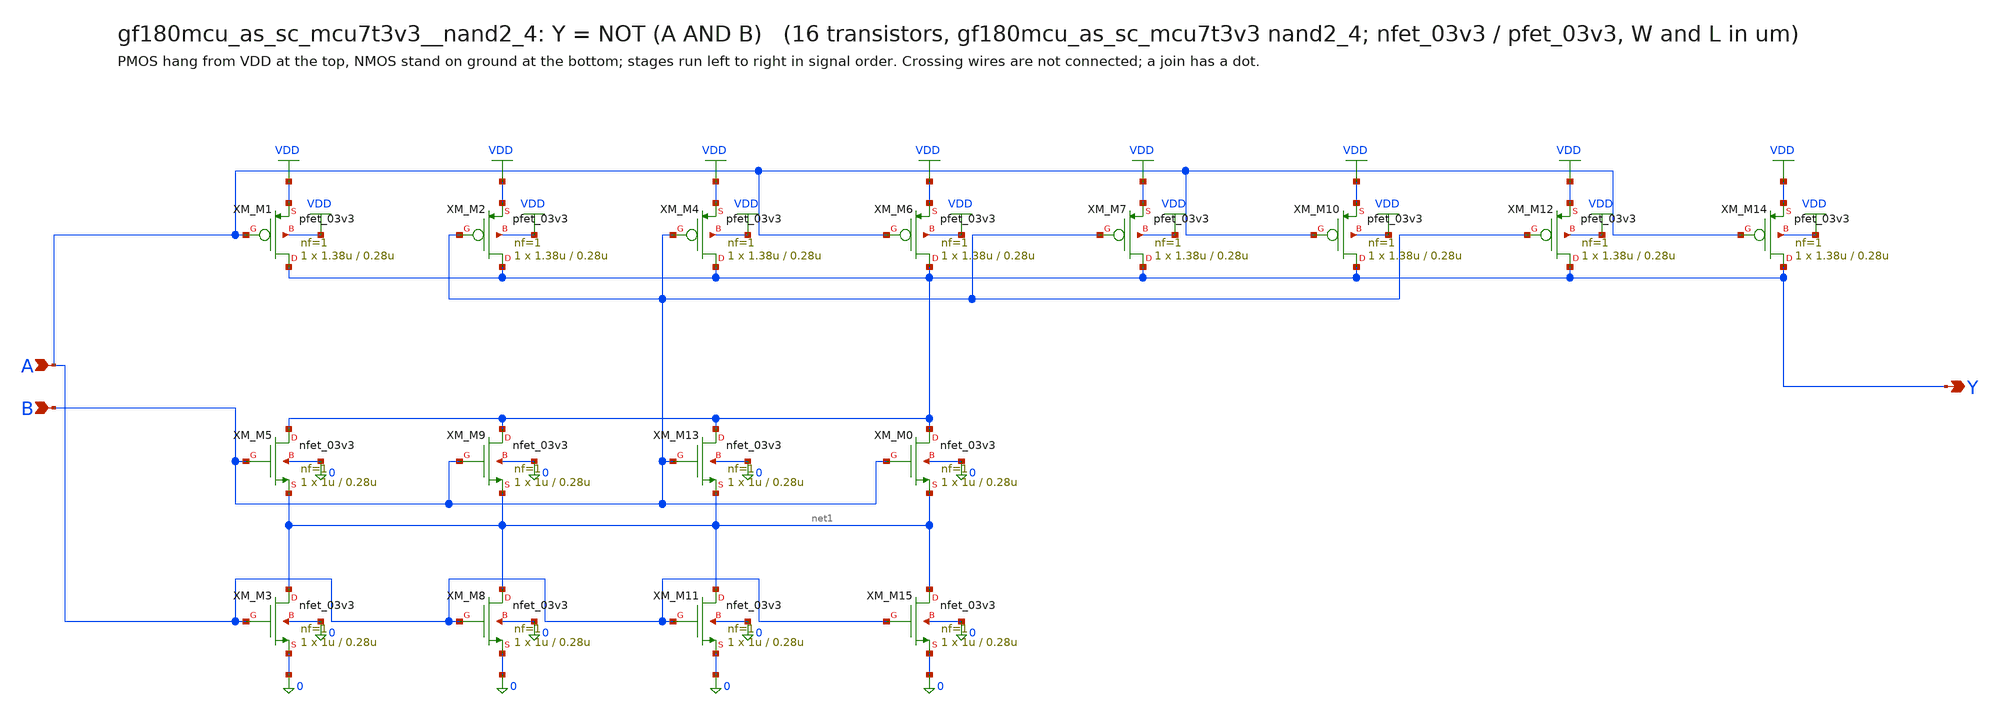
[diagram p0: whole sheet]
** sch_path: xschem/cells_tx/gf180mcu_as_sc_mcu7t3v3__nand2_4.sch
**.subckt gf180mcu_as_sc_mcu7t3v3__nand2_4 A B Y
*.ipin A
*.ipin B
*.opin Y
XM_M0 Y B net1 0 nfet_03v3 L=0.28u W=1u nf=1 ad=2.6e-13 as=2.6e-13 pd=1.52e-06 ps=1.52e-06 nrd=0
+ nrs=0 sa=0 sb=0 sd=0 m=1
XM_M1 Y A VDD VDD pfet_03v3 L=0.28u W=1.38u nf=1 ad=3.588e-13 as=3.588e-13 pd=1.9e-06 ps=1.9e-06
+ nrd=0 nrs=0 sa=0 sb=0 sd=0 m=1
XM_M2 Y B VDD VDD pfet_03v3 L=0.28u W=1.38u nf=1 ad=3.588e-13 as=3.588e-13 pd=1.9e-06 ps=1.9e-06
+ nrd=0 nrs=0 sa=0 sb=0 sd=0 m=1
XM_M3 net1 A 0 0 nfet_03v3 L=0.28u W=1u nf=1 ad=2.6e-13 as=4.4e-13 pd=1.52e-06 ps=2.88e-06 nrd=0
+ nrs=0 sa=0 sb=0 sd=0 m=1
XM_M4 Y B VDD VDD pfet_03v3 L=0.28u W=1.38u nf=1 ad=9.384e-13 as=3.588e-13 pd=4.12e-06 ps=1.9e-06
+ nrd=0 nrs=0 sa=0 sb=0 sd=0 m=1
XM_M5 Y B net1 0 nfet_03v3 L=0.28u W=1u nf=1 ad=2.6e-13 as=2.6e-13 pd=1.52e-06 ps=1.52e-06 nrd=0
+ nrs=0 sa=0 sb=0 sd=0 m=1
XM_M6 Y A VDD VDD pfet_03v3 L=0.28u W=1.38u nf=1 ad=3.588e-13 as=3.588e-13 pd=1.9e-06 ps=1.9e-06
+ nrd=0 nrs=0 sa=0 sb=0 sd=0 m=1
XM_M7 Y B VDD VDD pfet_03v3 L=0.28u W=1.38u nf=1 ad=3.588e-13 as=3.588e-13 pd=1.9e-06 ps=1.9e-06
+ nrd=0 nrs=0 sa=0 sb=0 sd=0 m=1
XM_M8 net1 A 0 0 nfet_03v3 L=0.28u W=1u nf=1 ad=2.6e-13 as=2.6e-13 pd=1.52e-06 ps=1.52e-06 nrd=0
+ nrs=0 sa=0 sb=0 sd=0 m=1
XM_M9 Y B net1 0 nfet_03v3 L=0.28u W=1u nf=1 ad=6.8e-13 as=2.6e-13 pd=3.36e-06 ps=1.52e-06 nrd=0
+ nrs=0 sa=0 sb=0 sd=0 m=1
XM_M10 Y A VDD VDD pfet_03v3 L=0.28u W=1.38u nf=1 ad=3.588e-13 as=3.588e-13 pd=1.9e-06 ps=1.9e-06
+ nrd=0 nrs=0 sa=0 sb=0 sd=0 m=1
XM_M11 net1 A 0 0 nfet_03v3 L=0.28u W=1u nf=1 ad=2.6e-13 as=2.6e-13 pd=1.52e-06 ps=1.52e-06 nrd=0
+ nrs=0 sa=0 sb=0 sd=0 m=1
XM_M12 Y B VDD VDD pfet_03v3 L=0.28u W=1.38u nf=1 ad=3.588e-13 as=3.588e-13 pd=1.9e-06 ps=1.9e-06
+ nrd=0 nrs=0 sa=0 sb=0 sd=0 m=1
XM_M13 Y B net1 0 nfet_03v3 L=0.28u W=1u nf=1 ad=2.6e-13 as=2.6e-13 pd=1.52e-06 ps=1.52e-06 nrd=0
+ nrs=0 sa=0 sb=0 sd=0 m=1
XM_M14 Y A VDD VDD pfet_03v3 L=0.28u W=1.38u nf=1 ad=3.588e-13 as=6.072e-13 pd=1.9e-06 ps=3.64e-06
+ nrd=0 nrs=0 sa=0 sb=0 sd=0 m=1
XM_M15 net1 A 0 0 nfet_03v3 L=0.28u W=1u nf=1 ad=2.6e-13 as=2.6e-13 pd=1.52e-06 ps=1.52e-06 nrd=0
+ nrs=0 sa=0 sb=0 sd=0 m=1
**.ends
.GLOBAL VDD
.end
